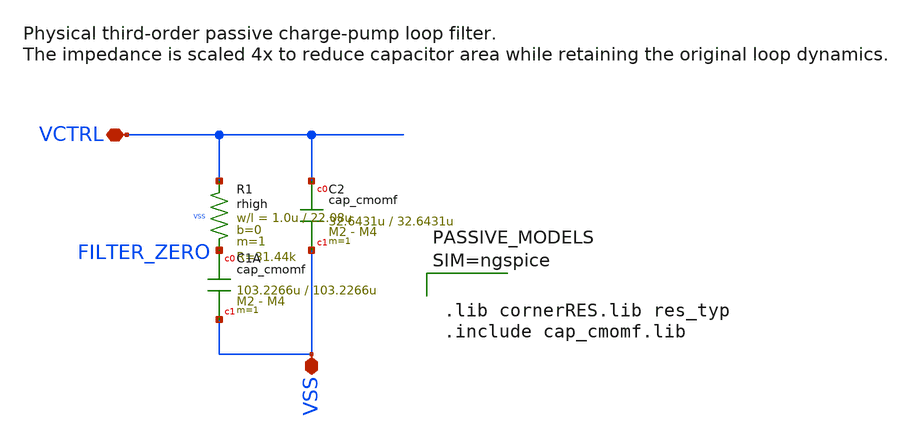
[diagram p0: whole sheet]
** sch_path: schematic/xschem/pll/loop_filter.sch
**.subckt loop_filter VCTRL VSS
*.iopin VCTRL
*.iopin VSS
XR1 VCTRL FILTER_ZERO VSS rhigh w=1.0u l=22.08u m=1 b=0 mm_ok=1
XC1A FILTER_ZERO VSS cap_cmomf w=103.2266u l=103.2266u mmin=2 mmax=4 subblock=0 rfmodel=0 subscale=1
+ m=1 mm_ok=1
XC2 VCTRL VSS cap_cmomf w=32.6431u l=32.6431u mmin=2 mmax=4 subblock=0 rfmodel=0 subscale=1 m=1
+ mm_ok=1
**** begin user architecture code



.lib cornerRES.lib res_typ
.include cap_cmomf.lib



**** end user architecture code
**.ends
.end
